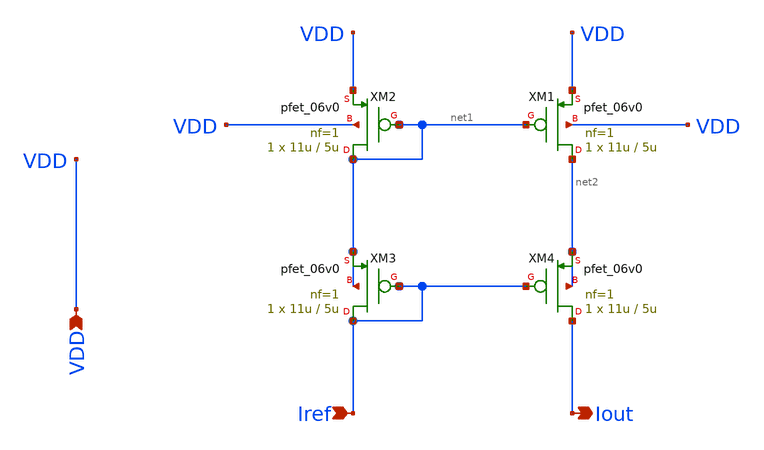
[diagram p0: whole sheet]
** sch_path: designs/libs/core_analog/pmos_current_mirror/pmos_current_mirror.sch
**.subckt pmos_current_mirror VDD Iref Iout
*.ipin VDD
*.ipin Iref
*.opin Iout
XM2 net1 net1 VDD VDD pfet_06v0 L=5u W=11u nf=1 ad='int((nf+1)/2) * W/nf * 0.18u' as='int((nf+2)/2) * W/nf * 0.18u'
+ pd='2*int((nf+1)/2) * (W/nf + 0.18u)' ps='2*int((nf+2)/2) * (W/nf + 0.18u)' nrd='0.18u / W' nrs='0.18u / W'
+ sa=0 sb=0 sd=0 m=1
XM1 net2 net1 VDD VDD pfet_06v0 L=5u W=11u nf=1 ad='int((nf+1)/2) * W/nf * 0.18u' as='int((nf+2)/2) * W/nf * 0.18u'
+ pd='2*int((nf+1)/2) * (W/nf + 0.18u)' ps='2*int((nf+2)/2) * (W/nf + 0.18u)' nrd='0.18u / W' nrs='0.18u / W'
+ sa=0 sb=0 sd=0 m=1
XM3 Iref Iref net1 net1 pfet_06v0 L=5u W=11u nf=1 ad='int((nf+1)/2) * W/nf * 0.18u' as='int((nf+2)/2) * W/nf * 0.18u'
+ pd='2*int((nf+1)/2) * (W/nf + 0.18u)' ps='2*int((nf+2)/2) * (W/nf + 0.18u)' nrd='0.18u / W' nrs='0.18u / W'
+ sa=0 sb=0 sd=0 m=1
XM4 Iout Iref net2 net2 pfet_06v0 L=5u W=11u nf=1 ad='int((nf+1)/2) * W/nf * 0.18u' as='int((nf+2)/2) * W/nf * 0.18u'
+ pd='2*int((nf+1)/2) * (W/nf + 0.18u)' ps='2*int((nf+2)/2) * (W/nf + 0.18u)' nrd='0.18u / W' nrs='0.18u / W'
+ sa=0 sb=0 sd=0 m=1
**.ends
.end
